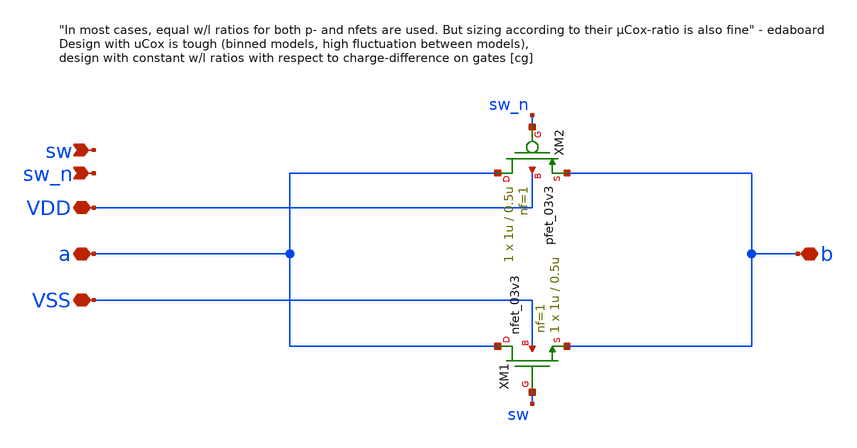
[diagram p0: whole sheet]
** sch_path: adc_sar_vcm_switch.sch
**.subckt adc_sar_vcm_switch VSS VDD sw_n sw a b
*.iopin VSS
*.iopin VDD
*.ipin sw_n
*.ipin sw
*.iopin a
*.iopin b
XM1 a sw b VSS nfet_03v3 L=0.5u W=1u nf=1 ad='int((nf+1)/2) * W/nf * 0.18u' as='int((nf+2)/2) * W/nf * 0.18u'
+ pd='2*int((nf+1)/2) * (W/nf + 0.18u)' ps='2*int((nf+2)/2) * (W/nf + 0.18u)' nrd='0.18u / W' nrs='0.18u / W'
+ sa=0 sb=0 sd=0 m=1
XM2 a sw_n b VDD pfet_03v3 L=0.5u W=1u nf=1 ad='int((nf+1)/2) * W/nf * 0.18u' as='int((nf+2)/2) * W/nf * 0.18u'
+ pd='2*int((nf+1)/2) * (W/nf + 0.18u)' ps='2*int((nf+2)/2) * (W/nf + 0.18u)' nrd='0.18u / W' nrs='0.18u / W'
+ sa=0 sb=0 sd=0 m=1
**.ends
.end
